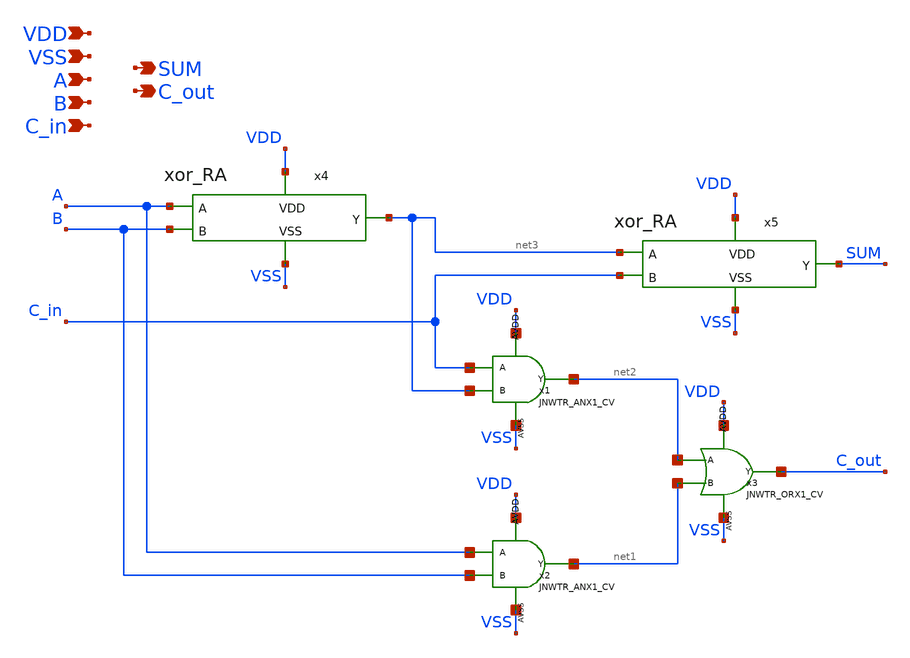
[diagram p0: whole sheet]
** sch_path: design/JNW_GR07_SKY130A/full_adder_RA.sch
**.subckt full_adder_RA VDD VSS A B SUM C_in C_out
*.ipin VDD
*.ipin VSS
*.ipin A
*.ipin B
*.opin SUM
*.ipin C_in
*.opin C_out
x1 C_in net3 net2 VDD VSS JNWTR_ANX1_CV xoffset=0 yoffset=0 angle=0 M=1
x2 A B net1 VDD VSS JNWTR_ANX1_CV xoffset=0 yoffset=0 angle=0 M=1
x3 net2 net1 C_out VDD VSS JNWTR_ORX1_CV xoffset=0 yoffset=0 angle=0 M=1
x4 VDD VSS net3 A B xor_RA
x5 VDD VSS SUM net3 C_in xor_RA
**.ends
.end
